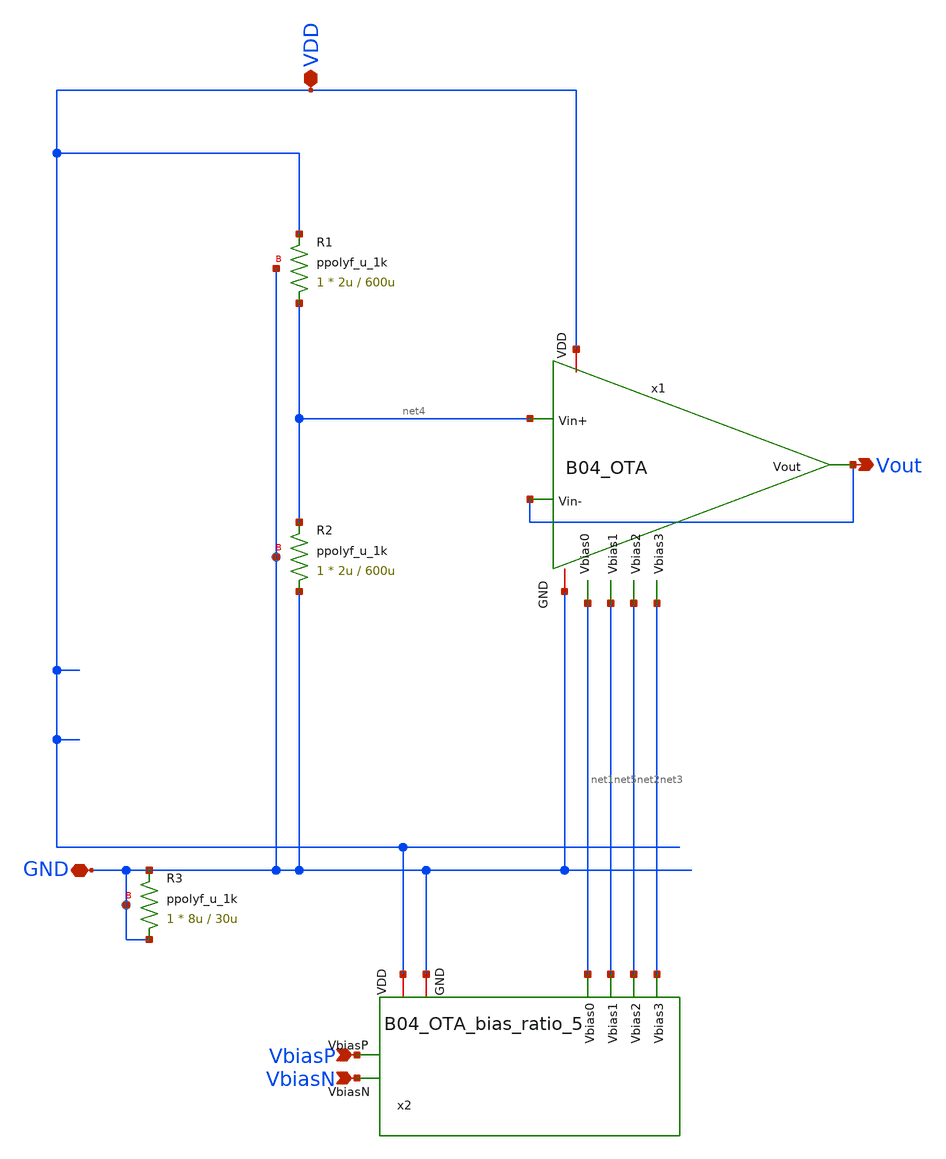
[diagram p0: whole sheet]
** sch_path: analog/B04_VDD05.sch
**.subckt B04_VDD05 VbiasP VbiasN GND VDD Vout
*.ipin VbiasP
*.ipin VbiasN
*.iopin GND
*.iopin VDD
*.opin Vout
XR1 net4 VDD GND ppolyf_u_1k r_width=2u r_length=600u m=1
XR2 GND net4 GND ppolyf_u_1k r_width=2u r_length=600u m=1
XR3 GND GND GND ppolyf_u_1k r_width=8u r_length=30u m=1
x1 VDD net1 net4 Vout net3 net5 Vout net2 GND B04_OTA
x2 VDD VbiasP net1 net2 net3 net5 VbiasN GND B04_OTA_bias_ratio_5
**.ends

* expanding   symbol:
*+  AURA-Event-Driven-Mixed-Signal-ASIC-for-Acoustic-Pattern-Detection/analog/B04_OTA.sym # of pins=9
** sym_path: analog/B04_OTA.sym
** sch_path: analog/B04_OTA.sch
.subckt B04_OTA VDD Vbias0 Vin+ Vin- Vbias3 Vbias1 Vout Vbias2 GND
*.iopin VDD
*.ipin Vbias0
*.ipin Vin+
*.ipin Vin-
*.opin Vout
*.ipin Vbias3
*.ipin Vbias2
*.iopin GND
*.ipin Vbias1
XM1 net1 Vbias0 VDD VDD pfet_03v3 L=4u W=5u nf=2 ad='int((nf+1)/2) * W/nf * 0.18u' as='int((nf+2)/2) * W/nf * 0.18u'
+ pd='2*int((nf+1)/2) * (W/nf + 0.18u)' ps='2*int((nf+2)/2) * (W/nf + 0.18u)' nrd='0.18u / W' nrs='0.18u / W'
+ sa=0 sb=0 sd=0 m=1
XM2 net6 Vin+ net1 VDD pfet_03v3 L=1u W=2u nf=4 ad='int((nf+1)/2) * W/nf * 0.18u' as='int((nf+2)/2) * W/nf * 0.18u'
+ pd='2*int((nf+1)/2) * (W/nf + 0.18u)' ps='2*int((nf+2)/2) * (W/nf + 0.18u)' nrd='0.18u / W' nrs='0.18u / W'
+ sa=0 sb=0 sd=0 m=1
XM3 net7 Vin- net1 VDD pfet_03v3 L=1u W=2u nf=4 ad='int((nf+1)/2) * W/nf * 0.18u' as='int((nf+2)/2) * W/nf * 0.18u'
+ pd='2*int((nf+1)/2) * (W/nf + 0.18u)' ps='2*int((nf+2)/2) * (W/nf + 0.18u)' nrd='0.18u / W' nrs='0.18u / W'
+ sa=0 sb=0 sd=0 m=1
XM4 net2 Vin+ net1 VDD pfet_03v3 L=1u W=2u nf=4 ad='int((nf+1)/2) * W/nf * 0.18u' as='int((nf+2)/2) * W/nf * 0.18u'
+ pd='2*int((nf+1)/2) * (W/nf + 0.18u)' ps='2*int((nf+2)/2) * (W/nf + 0.18u)' nrd='0.18u / W' nrs='0.18u / W'
+ sa=0 sb=0 sd=0 m=1
XM5 net3 Vin- net1 VDD pfet_03v3 L=1u W=2u nf=4 ad='int((nf+1)/2) * W/nf * 0.18u' as='int((nf+2)/2) * W/nf * 0.18u'
+ pd='2*int((nf+1)/2) * (W/nf + 0.18u)' ps='2*int((nf+2)/2) * (W/nf + 0.18u)' nrd='0.18u / W' nrs='0.18u / W'
+ sa=0 sb=0 sd=0 m=1
XM6 net2 Vbias2 net5 GND nfet_03v3 L=1u W=1u nf=1 ad='int((nf+1)/2) * W/nf * 0.18u' as='int((nf+2)/2) * W/nf * 0.18u'
+ pd='2*int((nf+1)/2) * (W/nf + 0.18u)' ps='2*int((nf+2)/2) * (W/nf + 0.18u)' nrd='0.18u / W' nrs='0.18u / W'
+ sa=0 sb=0 sd=0 m=2
XM7 net3 Vbias2 net4 GND nfet_03v3 L=1u W=1u nf=1 ad='int((nf+1)/2) * W/nf * 0.18u' as='int((nf+2)/2) * W/nf * 0.18u'
+ pd='2*int((nf+1)/2) * (W/nf + 0.18u)' ps='2*int((nf+2)/2) * (W/nf + 0.18u)' nrd='0.18u / W' nrs='0.18u / W'
+ sa=0 sb=0 sd=0 m=2
XM8 net5 net2 GND GND nfet_03v3 L=4u W=0.5u nf=1 ad='int((nf+1)/2) * W/nf * 0.18u' as='int((nf+2)/2) * W/nf * 0.18u'
+ pd='2*int((nf+1)/2) * (W/nf + 0.18u)' ps='2*int((nf+2)/2) * (W/nf + 0.18u)' nrd='0.18u / W' nrs='0.18u / W'
+ sa=0 sb=0 sd=0 m=2
XM9 net6 net3 GND GND nfet_03v3 L=4u W=0.5u nf=1 ad='int((nf+1)/2) * W/nf * 0.18u' as='int((nf+2)/2) * W/nf * 0.18u'
+ pd='2*int((nf+1)/2) * (W/nf + 0.18u)' ps='2*int((nf+2)/2) * (W/nf + 0.18u)' nrd='0.18u / W' nrs='0.18u / W'
+ sa=0 sb=0 sd=0 m=2
XM10 net4 net3 GND GND nfet_03v3 L=4u W=0.5u nf=1 ad='int((nf+1)/2) * W/nf * 0.18u' as='int((nf+2)/2) * W/nf * 0.18u'
+ pd='2*int((nf+1)/2) * (W/nf + 0.18u)' ps='2*int((nf+2)/2) * (W/nf + 0.18u)' nrd='0.18u / W' nrs='0.18u / W'
+ sa=0 sb=0 sd=0 m=2
XM11 net7 net2 GND GND nfet_03v3 L=4u W=0.5u nf=1 ad='int((nf+1)/2) * W/nf * 0.18u' as='int((nf+2)/2) * W/nf * 0.18u'
+ pd='2*int((nf+1)/2) * (W/nf + 0.18u)' ps='2*int((nf+2)/2) * (W/nf + 0.18u)' nrd='0.18u / W' nrs='0.18u / W'
+ sa=0 sb=0 sd=0 m=2
XM12 net9 net10 VDD VDD pfet_03v3 L=4u W=2.5u nf=1 ad='int((nf+1)/2) * W/nf * 0.18u' as='int((nf+2)/2) * W/nf * 0.18u'
+ pd='2*int((nf+1)/2) * (W/nf + 0.18u)' ps='2*int((nf+2)/2) * (W/nf + 0.18u)' nrd='0.18u / W' nrs='0.18u / W'
+ sa=0 sb=0 sd=0 m=2
XM13 net8 net10 VDD VDD pfet_03v3 L=4u W=2.5u nf=1 ad='int((nf+1)/2) * W/nf * 0.18u' as='int((nf+2)/2) * W/nf * 0.18u'
+ pd='2*int((nf+1)/2) * (W/nf + 0.18u)' ps='2*int((nf+2)/2) * (W/nf + 0.18u)' nrd='0.18u / W' nrs='0.18u / W'
+ sa=0 sb=0 sd=0 m=2
XM14 Vout Vbias3 net9 VDD pfet_03v3 L=4u W=2.5u nf=1 ad='int((nf+1)/2) * W/nf * 0.18u' as='int((nf+2)/2) * W/nf * 0.18u'
+ pd='2*int((nf+1)/2) * (W/nf + 0.18u)' ps='2*int((nf+2)/2) * (W/nf + 0.18u)' nrd='0.18u / W' nrs='0.18u / W'
+ sa=0 sb=0 sd=0 m=2
XM15 net10 Vbias3 net8 VDD pfet_03v3 L=4u W=2.5u nf=1 ad='int((nf+1)/2) * W/nf * 0.18u' as='int((nf+2)/2) * W/nf * 0.18u'
+ pd='2*int((nf+1)/2) * (W/nf + 0.18u)' ps='2*int((nf+2)/2) * (W/nf + 0.18u)' nrd='0.18u / W' nrs='0.18u / W'
+ sa=0 sb=0 sd=0 m=2
XM16 Vout Vbias2 net7 GND nfet_03v3 L=4u W=0.5u nf=1 ad='int((nf+1)/2) * W/nf * 0.18u' as='int((nf+2)/2) * W/nf * 0.18u'
+ pd='2*int((nf+1)/2) * (W/nf + 0.18u)' ps='2*int((nf+2)/2) * (W/nf + 0.18u)' nrd='0.18u / W' nrs='0.18u / W'
+ sa=0 sb=0 sd=0 m=2
XM17 net10 Vbias2 net6 GND nfet_03v3 L=4u W=0.5u nf=1 ad='int((nf+1)/2) * W/nf * 0.18u' as='int((nf+2)/2) * W/nf * 0.18u'
+ pd='2*int((nf+1)/2) * (W/nf + 0.18u)' ps='2*int((nf+2)/2) * (W/nf + 0.18u)' nrd='0.18u / W' nrs='0.18u / W'
+ sa=0 sb=0 sd=0 m=2
XM18 net6 Vbias1 GND GND nfet_03v3 L=4u W=0.5u nf=2 ad='int((nf+1)/2) * W/nf * 0.18u' as='int((nf+2)/2) * W/nf * 0.18u'
+ pd='2*int((nf+1)/2) * (W/nf + 0.18u)' ps='2*int((nf+2)/2) * (W/nf + 0.18u)' nrd='0.18u / W' nrs='0.18u / W'
+ sa=0 sb=0 sd=0 m=2
XM19 net7 Vbias1 GND GND nfet_03v3 L=4u W=0.5u nf=2 ad='int((nf+1)/2) * W/nf * 0.18u' as='int((nf+2)/2) * W/nf * 0.18u'
+ pd='2*int((nf+1)/2) * (W/nf + 0.18u)' ps='2*int((nf+2)/2) * (W/nf + 0.18u)' nrd='0.18u / W' nrs='0.18u / W'
+ sa=0 sb=0 sd=0 m=2
XMdummy VDD VDD VDD VDD pfet_03v3 L=1u W=0.5u nf=1 ad='int((nf+1)/2) * W/nf * 0.18u' as='int((nf+2)/2) * W/nf * 0.18u'
+ pd='2*int((nf+1)/2) * (W/nf + 0.18u)' ps='2*int((nf+2)/2) * (W/nf + 0.18u)' nrd='0.18u / W' nrs='0.18u / W'
+ sa=0 sb=0 sd=0 m=1
XMdummy1 VDD VDD VDD VDD pfet_03v3 L=1u W=0.5u nf=1 ad='int((nf+1)/2) * W/nf * 0.18u' as='int((nf+2)/2) * W/nf * 0.18u'
+ pd='2*int((nf+1)/2) * (W/nf + 0.18u)' ps='2*int((nf+2)/2) * (W/nf + 0.18u)' nrd='0.18u / W' nrs='0.18u / W'
+ sa=0 sb=0 sd=0 m=1
XMdummy2 VDD VDD VDD VDD pfet_03v3 L=1u W=0.5u nf=1 ad='int((nf+1)/2) * W/nf * 0.18u' as='int((nf+2)/2) * W/nf * 0.18u'
+ pd='2*int((nf+1)/2) * (W/nf + 0.18u)' ps='2*int((nf+2)/2) * (W/nf + 0.18u)' nrd='0.18u / W' nrs='0.18u / W'
+ sa=0 sb=0 sd=0 m=1
XMdummy3 VDD VDD VDD VDD pfet_03v3 L=1u W=0.5u nf=1 ad='int((nf+1)/2) * W/nf * 0.18u' as='int((nf+2)/2) * W/nf * 0.18u'
+ pd='2*int((nf+1)/2) * (W/nf + 0.18u)' ps='2*int((nf+2)/2) * (W/nf + 0.18u)' nrd='0.18u / W' nrs='0.18u / W'
+ sa=0 sb=0 sd=0 m=1
XMdummy4 VDD VDD VDD VDD pfet_03v3 L=4u W=2.5u nf=1 ad='int((nf+1)/2) * W/nf * 0.18u' as='int((nf+2)/2) * W/nf * 0.18u'
+ pd='2*int((nf+1)/2) * (W/nf + 0.18u)' ps='2*int((nf+2)/2) * (W/nf + 0.18u)' nrd='0.18u / W' nrs='0.18u / W'
+ sa=0 sb=0 sd=0 m=1
XMdummy5 VDD VDD VDD VDD pfet_03v3 L=4u W=2.5u nf=1 ad='int((nf+1)/2) * W/nf * 0.18u' as='int((nf+2)/2) * W/nf * 0.18u'
+ pd='2*int((nf+1)/2) * (W/nf + 0.18u)' ps='2*int((nf+2)/2) * (W/nf + 0.18u)' nrd='0.18u / W' nrs='0.18u / W'
+ sa=0 sb=0 sd=0 m=1
XMdummy6 VDD VDD VDD VDD pfet_03v3 L=4u W=2.5u nf=1 ad='int((nf+1)/2) * W/nf * 0.18u' as='int((nf+2)/2) * W/nf * 0.18u'
+ pd='2*int((nf+1)/2) * (W/nf + 0.18u)' ps='2*int((nf+2)/2) * (W/nf + 0.18u)' nrd='0.18u / W' nrs='0.18u / W'
+ sa=0 sb=0 sd=0 m=1
XMdummy7 VDD VDD VDD VDD pfet_03v3 L=4u W=2.5u nf=1 ad='int((nf+1)/2) * W/nf * 0.18u' as='int((nf+2)/2) * W/nf * 0.18u'
+ pd='2*int((nf+1)/2) * (W/nf + 0.18u)' ps='2*int((nf+2)/2) * (W/nf + 0.18u)' nrd='0.18u / W' nrs='0.18u / W'
+ sa=0 sb=0 sd=0 m=1
XMdummy8 GND GND GND GND nfet_03v3 L=4u W=0.5u nf=1 ad='int((nf+1)/2) * W/nf * 0.18u' as='int((nf+2)/2) * W/nf * 0.18u'
+ pd='2*int((nf+1)/2) * (W/nf + 0.18u)' ps='2*int((nf+2)/2) * (W/nf + 0.18u)' nrd='0.18u / W' nrs='0.18u / W'
+ sa=0 sb=0 sd=0 m=1
XMdummy9 GND GND GND GND nfet_03v3 L=4u W=0.5u nf=1 ad='int((nf+1)/2) * W/nf * 0.18u' as='int((nf+2)/2) * W/nf * 0.18u'
+ pd='2*int((nf+1)/2) * (W/nf + 0.18u)' ps='2*int((nf+2)/2) * (W/nf + 0.18u)' nrd='0.18u / W' nrs='0.18u / W'
+ sa=0 sb=0 sd=0 m=1
XMdummy10 GND GND GND GND nfet_03v3 L=1u W=1u nf=1 ad='int((nf+1)/2) * W/nf * 0.18u' as='int((nf+2)/2) * W/nf * 0.18u'
+ pd='2*int((nf+1)/2) * (W/nf + 0.18u)' ps='2*int((nf+2)/2) * (W/nf + 0.18u)' nrd='0.18u / W' nrs='0.18u / W'
+ sa=0 sb=0 sd=0 m=1
XMdummy11 GND GND GND GND nfet_03v3 L=1u W=1u nf=1 ad='int((nf+1)/2) * W/nf * 0.18u' as='int((nf+2)/2) * W/nf * 0.18u'
+ pd='2*int((nf+1)/2) * (W/nf + 0.18u)' ps='2*int((nf+2)/2) * (W/nf + 0.18u)' nrd='0.18u / W' nrs='0.18u / W'
+ sa=0 sb=0 sd=0 m=1
XMdummy12 GND GND GND GND nfet_03v3 L=1u W=1u nf=1 ad='int((nf+1)/2) * W/nf * 0.18u' as='int((nf+2)/2) * W/nf * 0.18u'
+ pd='2*int((nf+1)/2) * (W/nf + 0.18u)' ps='2*int((nf+2)/2) * (W/nf + 0.18u)' nrd='0.18u / W' nrs='0.18u / W'
+ sa=0 sb=0 sd=0 m=1
XMdummy13 GND GND GND GND nfet_03v3 L=1u W=1u nf=1 ad='int((nf+1)/2) * W/nf * 0.18u' as='int((nf+2)/2) * W/nf * 0.18u'
+ pd='2*int((nf+1)/2) * (W/nf + 0.18u)' ps='2*int((nf+2)/2) * (W/nf + 0.18u)' nrd='0.18u / W' nrs='0.18u / W'
+ sa=0 sb=0 sd=0 m=1
XMdummy16 GND GND GND GND nfet_03v3 L=4u W=0.5u nf=1 ad='int((nf+1)/2) * W/nf * 0.18u' as='int((nf+2)/2) * W/nf * 0.18u'
+ pd='2*int((nf+1)/2) * (W/nf + 0.18u)' ps='2*int((nf+2)/2) * (W/nf + 0.18u)' nrd='0.18u / W' nrs='0.18u / W'
+ sa=0 sb=0 sd=0 m=1
XMdummy17 GND GND GND GND nfet_03v3 L=4u W=0.5u nf=1 ad='int((nf+1)/2) * W/nf * 0.18u' as='int((nf+2)/2) * W/nf * 0.18u'
+ pd='2*int((nf+1)/2) * (W/nf + 0.18u)' ps='2*int((nf+2)/2) * (W/nf + 0.18u)' nrd='0.18u / W' nrs='0.18u / W'
+ sa=0 sb=0 sd=0 m=1
XMdummy18 GND GND GND GND nfet_03v3 L=4u W=0.5u nf=1 ad='int((nf+1)/2) * W/nf * 0.18u' as='int((nf+2)/2) * W/nf * 0.18u'
+ pd='2*int((nf+1)/2) * (W/nf + 0.18u)' ps='2*int((nf+2)/2) * (W/nf + 0.18u)' nrd='0.18u / W' nrs='0.18u / W'
+ sa=0 sb=0 sd=0 m=1
XMdummy19 GND GND GND GND nfet_03v3 L=4u W=0.5u nf=1 ad='int((nf+1)/2) * W/nf * 0.18u' as='int((nf+2)/2) * W/nf * 0.18u'
+ pd='2*int((nf+1)/2) * (W/nf + 0.18u)' ps='2*int((nf+2)/2) * (W/nf + 0.18u)' nrd='0.18u / W' nrs='0.18u / W'
+ sa=0 sb=0 sd=0 m=1
.ends


* expanding   symbol:
*+  AURA-Event-Driven-Mixed-Signal-ASIC-for-Acoustic-Pattern-Detection/analog/B04_OTA_bias_ratio_5.sym # of pins=8
** sym_path: analog/B04_OTA_bias_ratio_5.sym
** sch_path: analog/B04_OTA_bias_ratio_5.sch
.subckt B04_OTA_bias_ratio_5 VDD VbiasP Vbias0 Vbias2 Vbias3 Vbias1 VbiasN GND
*.iopin VDD
*.opin Vbias2
*.opin Vbias1
*.opin Vbias0
*.opin Vbias3
*.iopin GND
*.ipin VbiasP
*.ipin VbiasN
XM1 Vbias1 GND Vbias2 VDD pfet_03v3 L=4u W=5u nf=1 ad='int((nf+1)/2) * W/nf * 0.18u' as='int((nf+2)/2) * W/nf * 0.18u'
+ pd='2*int((nf+1)/2) * (W/nf + 0.18u)' ps='2*int((nf+2)/2) * (W/nf + 0.18u)' nrd='0.18u / W' nrs='0.18u / W'
+ sa=0 sb=0 sd=0 m=1
XM4 Vbias1 Vbias2 net1 GND nfet_03v3 L=4u W=1u nf=1 ad='int((nf+1)/2) * W/nf * 0.18u' as='int((nf+2)/2) * W/nf * 0.18u'
+ pd='2*int((nf+1)/2) * (W/nf + 0.18u)' ps='2*int((nf+2)/2) * (W/nf + 0.18u)' nrd='0.18u / W' nrs='0.18u / W'
+ sa=0 sb=0 sd=0 m=1
XM5 net1 Vbias1 GND GND nfet_03v3 L=4u W=1u nf=1 ad='int((nf+1)/2) * W/nf * 0.18u' as='int((nf+2)/2) * W/nf * 0.18u'
+ pd='2*int((nf+1)/2) * (W/nf + 0.18u)' ps='2*int((nf+2)/2) * (W/nf + 0.18u)' nrd='0.18u / W' nrs='0.18u / W'
+ sa=0 sb=0 sd=0 m=1
XM9 net2 Vbias3 Vbias0 VDD pfet_03v3 L=4u W=5u nf=1 ad='int((nf+1)/2) * W/nf * 0.18u' as='int((nf+2)/2) * W/nf * 0.18u'
+ pd='2*int((nf+1)/2) * (W/nf + 0.18u)' ps='2*int((nf+2)/2) * (W/nf + 0.18u)' nrd='0.18u / W' nrs='0.18u / W'
+ sa=0 sb=0 sd=0 m=1
XM10 VDD Vbias0 net2 VDD pfet_03v3 L=4u W=5u nf=1 ad='int((nf+1)/2) * W/nf * 0.18u' as='int((nf+2)/2) * W/nf * 0.18u'
+ pd='2*int((nf+1)/2) * (W/nf + 0.18u)' ps='2*int((nf+2)/2) * (W/nf + 0.18u)' nrd='0.18u / W' nrs='0.18u / W'
+ sa=0 sb=0 sd=0 m=1
XM6 Vbias3 VDD Vbias0 GND nfet_03v3 L=4u W=10u nf=1 ad='int((nf+1)/2) * W/nf * 0.18u' as='int((nf+2)/2) * W/nf * 0.18u'
+ pd='2*int((nf+1)/2) * (W/nf + 0.18u)' ps='2*int((nf+2)/2) * (W/nf + 0.18u)' nrd='0.18u / W' nrs='0.18u / W'
+ sa=0 sb=0 sd=0 m=1
XM2 Vbias2 VbiasP VDD VDD pfet_03v3 L=4u W=25u nf=1 ad='int((nf+1)/2) * W/nf * 0.18u' as='int((nf+2)/2) * W/nf * 0.18u'
+ pd='2*int((nf+1)/2) * (W/nf + 0.18u)' ps='2*int((nf+2)/2) * (W/nf + 0.18u)' nrd='0.18u / W' nrs='0.18u / W'
+ sa=0 sb=0 sd=0 m=1
XM3 GND VbiasN Vbias3 GND nfet_03v3 L=4u W=50u nf=1 ad='int((nf+1)/2) * W/nf * 0.18u' as='int((nf+2)/2) * W/nf * 0.18u'
+ pd='2*int((nf+1)/2) * (W/nf + 0.18u)' ps='2*int((nf+2)/2) * (W/nf + 0.18u)' nrd='0.18u / W' nrs='0.18u / W'
+ sa=0 sb=0 sd=0 m=1
.ends

.end
